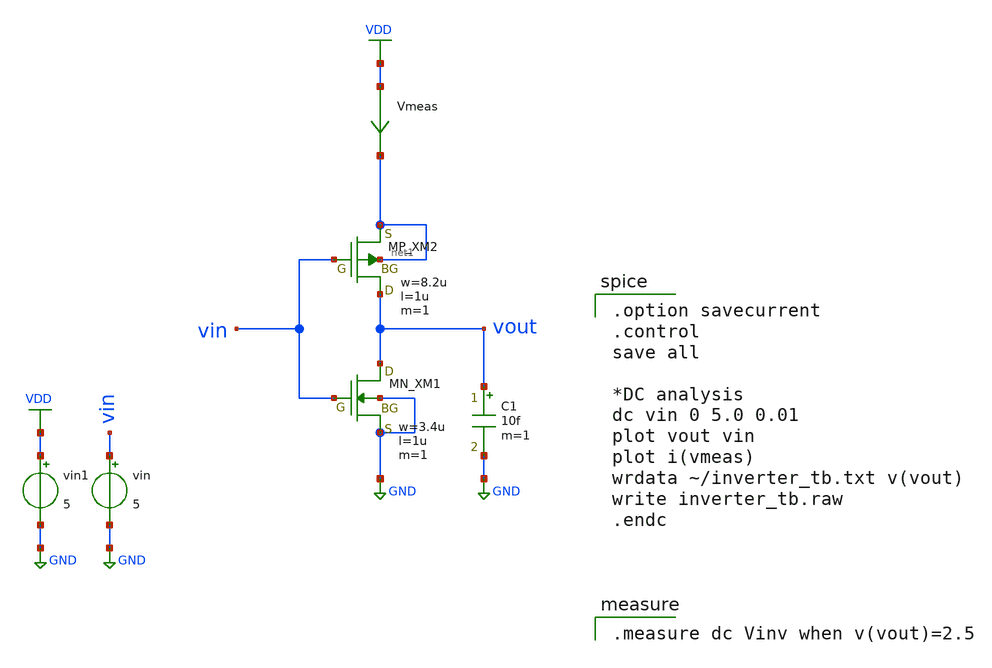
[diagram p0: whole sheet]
** sch_path: sim.sch
**.subckt sim
XXM1 vout vin GND GND NMOS w=3.4u l=1u nrd=0 nrs=0 m=1
XXM2 vout vin net1 net1 PMOS w=8.2u l=1u nrd=0 nrs=0 m=1
C1 vout GND 10f m=1
vin vin GND 5
Vmeas VDD net1 0
.save i(vmeas)
vin1 VDD GND 5
**** begin user architecture code
 .include $::LIB/ip62_models

.option savecurrent
.control
save all

*DC analysis
dc vin 0 5.0 0.01
plot vout vin
plot i(vmeas)
wrdata ~/inverter_tb.txt v(vout)
write inverter_tb.raw
.endc



.measure dc Vinv when v(vout)=2.5

**** end user architecture code
**.ends
.GLOBAL VDD
.GLOBAL GND
.end
